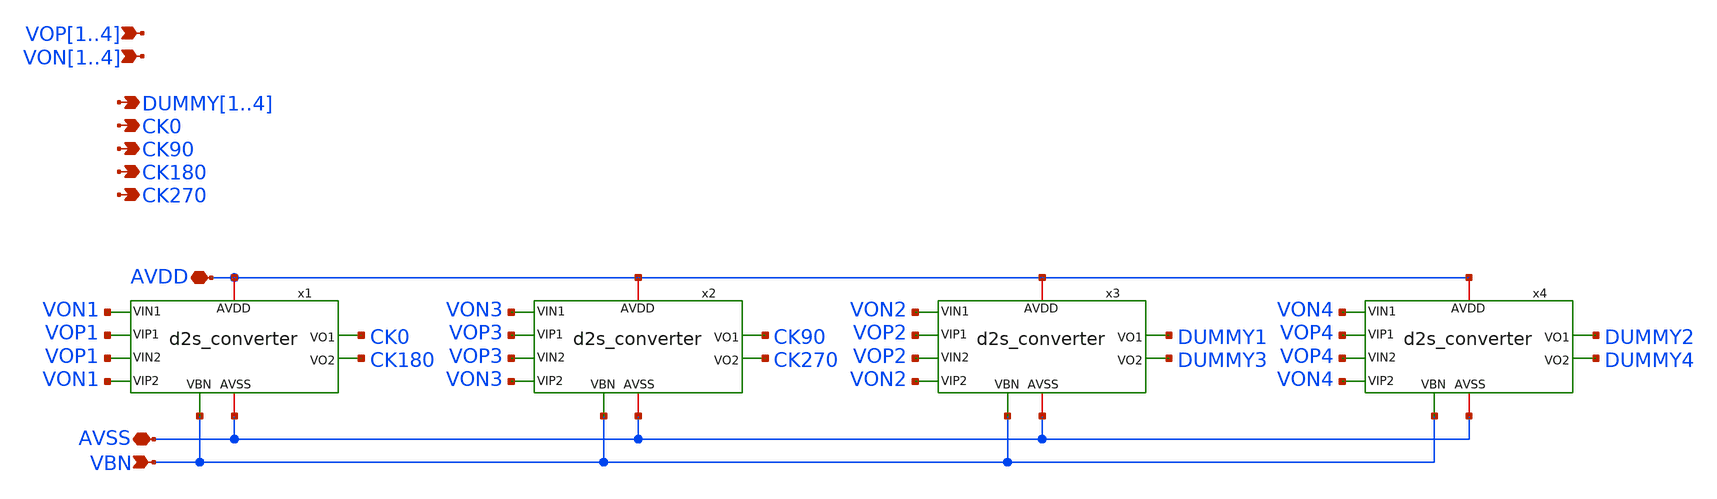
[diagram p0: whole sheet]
** sch_path: designs/libs/core_analog/d2s_top/d2s_top.sch
**.subckt d2s_top VOP1,VOP2,VOP3,VOP4 VON1,VON2,VON3,VON4 VBN DUMMY1,DUMMY2,DUMMY3,DUMMY4 CK0 CK90
*+ CK180 CK270 AVDD AVSS
*.ipin VOP1,VOP2,VOP3,VOP4
*.ipin VON1,VON2,VON3,VON4
*.ipin VBN
*.opin DUMMY1,DUMMY2,DUMMY3,DUMMY4
*.opin CK0
*.opin CK90
*.opin CK180
*.opin CK270
*.iopin AVDD
*.iopin AVSS
x1 AVDD AVSS VON1 VOP1 VBN CK0 VOP1 VON1 CK180 d2s_converter
x2 AVDD AVSS VON3 VOP3 VBN CK90 VOP3 VON3 CK270 d2s_converter
x3 AVDD AVSS VON2 VOP2 VBN DUMMY1 VOP2 VON2 DUMMY3 d2s_converter
x4 AVDD AVSS VON4 VOP4 VBN DUMMY2 VOP4 VON4 DUMMY4 d2s_converter
**.ends

* expanding   symbol:  libs/core_analog/d2s_converter/d2s_converter.sym # of pins=9
** sym_path: designs/libs/core_analog/d2s_converter/d2s_converter.sym
** sch_path: designs/libs/core_analog/d2s_converter/d2s_converter.sch
.subckt d2s_converter AVDD AVSS VIN1 VIP1 VBN VO1 VIN2 VIP2 VO2
*.iopin AVDD
*.iopin AVSS
*.ipin VIN1
*.ipin VIP1
*.opin VO1
*.ipin VBN
*.opin VO2
*.ipin VIN2
*.ipin VIP2
XM2 VOPB1 VIN1 i1 AVSS nfet_03v3 L=0.3u W=0.95u nf=1 ad='int((nf+1)/2) * W/nf * 0.18u' as='int((nf+2)/2) * W/nf * 0.18u'
+ pd='2*int((nf+1)/2) * (W/nf + 0.18u)' ps='2*int((nf+2)/2) * (W/nf + 0.18u)' nrd='0.18u / W' nrs='0.18u / W'
+ sa=0 sb=0 sd=0 m=4
XM4 VOPB1 VOPB1 AVDD AVDD pfet_03v3 L=0.3u W=0.7u nf=1 ad='int((nf+1)/2) * W/nf * 0.18u' as='int((nf+2)/2) * W/nf * 0.18u'
+ pd='2*int((nf+1)/2) * (W/nf + 0.18u)' ps='2*int((nf+2)/2) * (W/nf + 0.18u)' nrd='0.18u / W' nrs='0.18u / W'
+ sa=0 sb=0 sd=0 m=4
XM11 VOB1 VOB1 AVSS AVSS nfet_03v3 L=0.3u W=0.75u nf=1 ad='int((nf+1)/2) * W/nf * 0.18u' as='int((nf+2)/2) * W/nf * 0.18u'
+ pd='2*int((nf+1)/2) * (W/nf + 0.18u)' ps='2*int((nf+2)/2) * (W/nf + 0.18u)' nrd='0.18u / W' nrs='0.18u / W'
+ sa=0 sb=0 sd=0 m=4
XM13 VOB1 VOP1 AVDD AVDD pfet_03v3 L=0.3u W=1u nf=1 ad='int((nf+1)/2) * W/nf * 0.18u' as='int((nf+2)/2) * W/nf * 0.18u'
+ pd='2*int((nf+1)/2) * (W/nf + 0.18u)' ps='2*int((nf+2)/2) * (W/nf + 0.18u)' nrd='0.18u / W' nrs='0.18u / W'
+ sa=0 sb=0 sd=0 m=4
XM1 i1 VBN AVSS AVSS nfet_03v3 L=0.5u W=2.82u nf=1 ad='int((nf+1)/2) * W/nf * 0.18u' as='int((nf+2)/2) * W/nf * 0.18u'
+ pd='2*int((nf+1)/2) * (W/nf + 0.18u)' ps='2*int((nf+2)/2) * (W/nf + 0.18u)' nrd='0.18u / W' nrs='0.18u / W'
+ sa=0 sb=0 sd=0 m=4
x2 AVDD y VO2 AVSS inv
x1 AVDD x VO1 AVSS inv
XM3 VOP1 VIP1 i1 AVSS nfet_03v3 L=0.3u W=0.95u nf=1 ad='int((nf+1)/2) * W/nf * 0.18u' as='int((nf+2)/2) * W/nf * 0.18u'
+ pd='2*int((nf+1)/2) * (W/nf + 0.18u)' ps='2*int((nf+2)/2) * (W/nf + 0.18u)' nrd='0.18u / W' nrs='0.18u / W'
+ sa=0 sb=0 sd=0 m=4
XM7 VONB1 VIP1 i2 AVSS nfet_03v3 L=0.3u W=0.95u nf=1 ad='int((nf+1)/2) * W/nf * 0.18u' as='int((nf+2)/2) * W/nf * 0.18u'
+ pd='2*int((nf+1)/2) * (W/nf + 0.18u)' ps='2*int((nf+2)/2) * (W/nf + 0.18u)' nrd='0.18u / W' nrs='0.18u / W'
+ sa=0 sb=0 sd=0 m=4
XM9 VON1 VIN1 i2 AVSS nfet_03v3 L=0.3u W=0.95u nf=1 ad='int((nf+1)/2) * W/nf * 0.18u' as='int((nf+2)/2) * W/nf * 0.18u'
+ pd='2*int((nf+1)/2) * (W/nf + 0.18u)' ps='2*int((nf+2)/2) * (W/nf + 0.18u)' nrd='0.18u / W' nrs='0.18u / W'
+ sa=0 sb=0 sd=0 m=4
XM5 VOP1 VOPB1 AVDD AVDD pfet_03v3 L=0.3u W=0.7u nf=1 ad='int((nf+1)/2) * W/nf * 0.18u' as='int((nf+2)/2) * W/nf * 0.18u'
+ pd='2*int((nf+1)/2) * (W/nf + 0.18u)' ps='2*int((nf+2)/2) * (W/nf + 0.18u)' nrd='0.18u / W' nrs='0.18u / W'
+ sa=0 sb=0 sd=0 m=4
XM8 VONB1 VONB1 AVDD AVDD pfet_03v3 L=0.3u W=0.7u nf=1 ad='int((nf+1)/2) * W/nf * 0.18u' as='int((nf+2)/2) * W/nf * 0.18u'
+ pd='2*int((nf+1)/2) * (W/nf + 0.18u)' ps='2*int((nf+2)/2) * (W/nf + 0.18u)' nrd='0.18u / W' nrs='0.18u / W'
+ sa=0 sb=0 sd=0 m=4
XM10 VON1 VONB1 AVDD AVDD pfet_03v3 L=0.3u W=0.7u nf=1 ad='int((nf+1)/2) * W/nf * 0.18u' as='int((nf+2)/2) * W/nf * 0.18u'
+ pd='2*int((nf+1)/2) * (W/nf + 0.18u)' ps='2*int((nf+2)/2) * (W/nf + 0.18u)' nrd='0.18u / W' nrs='0.18u / W'
+ sa=0 sb=0 sd=0 m=4
XM15 VOPB2 VIN2 i3 AVSS nfet_03v3 L=0.3u W=0.95u nf=1 ad='int((nf+1)/2) * W/nf * 0.18u' as='int((nf+2)/2) * W/nf * 0.18u'
+ pd='2*int((nf+1)/2) * (W/nf + 0.18u)' ps='2*int((nf+2)/2) * (W/nf + 0.18u)' nrd='0.18u / W' nrs='0.18u / W'
+ sa=0 sb=0 sd=0 m=4
XM16 VOPB2 VOPB2 AVDD AVDD pfet_03v3 L=0.3u W=0.7u nf=1 ad='int((nf+1)/2) * W/nf * 0.18u' as='int((nf+2)/2) * W/nf * 0.18u'
+ pd='2*int((nf+1)/2) * (W/nf + 0.18u)' ps='2*int((nf+2)/2) * (W/nf + 0.18u)' nrd='0.18u / W' nrs='0.18u / W'
+ sa=0 sb=0 sd=0 m=4
XM21 VOP2 VIP2 i3 AVSS nfet_03v3 L=0.3u W=0.95u nf=1 ad='int((nf+1)/2) * W/nf * 0.18u' as='int((nf+2)/2) * W/nf * 0.18u'
+ pd='2*int((nf+1)/2) * (W/nf + 0.18u)' ps='2*int((nf+2)/2) * (W/nf + 0.18u)' nrd='0.18u / W' nrs='0.18u / W'
+ sa=0 sb=0 sd=0 m=4
XM22 VONB2 VIP2 i4 AVSS nfet_03v3 L=0.3u W=0.95u nf=1 ad='int((nf+1)/2) * W/nf * 0.18u' as='int((nf+2)/2) * W/nf * 0.18u'
+ pd='2*int((nf+1)/2) * (W/nf + 0.18u)' ps='2*int((nf+2)/2) * (W/nf + 0.18u)' nrd='0.18u / W' nrs='0.18u / W'
+ sa=0 sb=0 sd=0 m=4
XM23 VON2 VIN2 i4 AVSS nfet_03v3 L=0.3u W=0.95u nf=1 ad='int((nf+1)/2) * W/nf * 0.18u' as='int((nf+2)/2) * W/nf * 0.18u'
+ pd='2*int((nf+1)/2) * (W/nf + 0.18u)' ps='2*int((nf+2)/2) * (W/nf + 0.18u)' nrd='0.18u / W' nrs='0.18u / W'
+ sa=0 sb=0 sd=0 m=4
XM24 VOP2 VOPB2 AVDD AVDD pfet_03v3 L=0.3u W=0.7u nf=1 ad='int((nf+1)/2) * W/nf * 0.18u' as='int((nf+2)/2) * W/nf * 0.18u'
+ pd='2*int((nf+1)/2) * (W/nf + 0.18u)' ps='2*int((nf+2)/2) * (W/nf + 0.18u)' nrd='0.18u / W' nrs='0.18u / W'
+ sa=0 sb=0 sd=0 m=4
XM27 VONB2 VONB2 AVDD AVDD pfet_03v3 L=0.3u W=0.7u nf=1 ad='int((nf+1)/2) * W/nf * 0.18u' as='int((nf+2)/2) * W/nf * 0.18u'
+ pd='2*int((nf+1)/2) * (W/nf + 0.18u)' ps='2*int((nf+2)/2) * (W/nf + 0.18u)' nrd='0.18u / W' nrs='0.18u / W'
+ sa=0 sb=0 sd=0 m=4
XM28 VON2 VONB2 AVDD AVDD pfet_03v3 L=0.3u W=0.7u nf=1 ad='int((nf+1)/2) * W/nf * 0.18u' as='int((nf+2)/2) * W/nf * 0.18u'
+ pd='2*int((nf+1)/2) * (W/nf + 0.18u)' ps='2*int((nf+2)/2) * (W/nf + 0.18u)' nrd='0.18u / W' nrs='0.18u / W'
+ sa=0 sb=0 sd=0 m=4
XM12 x VOB1 AVSS AVSS nfet_03v3 L=0.3u W=0.75u nf=1 ad='int((nf+1)/2) * W/nf * 0.18u' as='int((nf+2)/2) * W/nf * 0.18u'
+ pd='2*int((nf+1)/2) * (W/nf + 0.18u)' ps='2*int((nf+2)/2) * (W/nf + 0.18u)' nrd='0.18u / W' nrs='0.18u / W'
+ sa=0 sb=0 sd=0 m=4
XM14 x VON1 AVDD AVDD pfet_03v3 L=0.3u W=1u nf=1 ad='int((nf+1)/2) * W/nf * 0.18u' as='int((nf+2)/2) * W/nf * 0.18u'
+ pd='2*int((nf+1)/2) * (W/nf + 0.18u)' ps='2*int((nf+2)/2) * (W/nf + 0.18u)' nrd='0.18u / W' nrs='0.18u / W'
+ sa=0 sb=0 sd=0 m=4
XM17 VOB2 VOB2 AVSS AVSS nfet_03v3 L=0.3u W=0.75u nf=1 ad='int((nf+1)/2) * W/nf * 0.18u' as='int((nf+2)/2) * W/nf * 0.18u'
+ pd='2*int((nf+1)/2) * (W/nf + 0.18u)' ps='2*int((nf+2)/2) * (W/nf + 0.18u)' nrd='0.18u / W' nrs='0.18u / W'
+ sa=0 sb=0 sd=0 m=4
XM18 VOB2 VOP2 AVDD AVDD pfet_03v3 L=0.3u W=1u nf=1 ad='int((nf+1)/2) * W/nf * 0.18u' as='int((nf+2)/2) * W/nf * 0.18u'
+ pd='2*int((nf+1)/2) * (W/nf + 0.18u)' ps='2*int((nf+2)/2) * (W/nf + 0.18u)' nrd='0.18u / W' nrs='0.18u / W'
+ sa=0 sb=0 sd=0 m=4
XM25 y VOB2 AVSS AVSS nfet_03v3 L=0.3u W=0.75u nf=1 ad='int((nf+1)/2) * W/nf * 0.18u' as='int((nf+2)/2) * W/nf * 0.18u'
+ pd='2*int((nf+1)/2) * (W/nf + 0.18u)' ps='2*int((nf+2)/2) * (W/nf + 0.18u)' nrd='0.18u / W' nrs='0.18u / W'
+ sa=0 sb=0 sd=0 m=4
XM26 y VON2 AVDD AVDD pfet_03v3 L=0.3u W=1u nf=1 ad='int((nf+1)/2) * W/nf * 0.18u' as='int((nf+2)/2) * W/nf * 0.18u'
+ pd='2*int((nf+1)/2) * (W/nf + 0.18u)' ps='2*int((nf+2)/2) * (W/nf + 0.18u)' nrd='0.18u / W' nrs='0.18u / W'
+ sa=0 sb=0 sd=0 m=4
XM6 i2 VBN AVSS AVSS nfet_03v3 L=0.5u W=2.82u nf=1 ad='int((nf+1)/2) * W/nf * 0.18u' as='int((nf+2)/2) * W/nf * 0.18u'
+ pd='2*int((nf+1)/2) * (W/nf + 0.18u)' ps='2*int((nf+2)/2) * (W/nf + 0.18u)' nrd='0.18u / W' nrs='0.18u / W'
+ sa=0 sb=0 sd=0 m=4
XM19 i3 VBN AVSS AVSS nfet_03v3 L=0.5u W=2.82u nf=1 ad='int((nf+1)/2) * W/nf * 0.18u' as='int((nf+2)/2) * W/nf * 0.18u'
+ pd='2*int((nf+1)/2) * (W/nf + 0.18u)' ps='2*int((nf+2)/2) * (W/nf + 0.18u)' nrd='0.18u / W' nrs='0.18u / W'
+ sa=0 sb=0 sd=0 m=4
XM20 i4 VBN AVSS AVSS nfet_03v3 L=0.5u W=2.82u nf=1 ad='int((nf+1)/2) * W/nf * 0.18u' as='int((nf+2)/2) * W/nf * 0.18u'
+ pd='2*int((nf+1)/2) * (W/nf + 0.18u)' ps='2*int((nf+2)/2) * (W/nf + 0.18u)' nrd='0.18u / W' nrs='0.18u / W'
+ sa=0 sb=0 sd=0 m=4
.ends


* expanding   symbol:  libs/core_analog/inv/inv.sym # of pins=4
** sym_path: designs/libs/core_analog/inv/inv.sym
** sch_path: designs/libs/core_analog/inv/inv.sch
.subckt inv AVDD IN OUT AVSS
*.ipin IN
*.iopin AVDD
*.iopin AVSS
*.opin OUT
XM1 OUT IN AVDD AVDD pfet_03v3 L=0.28u W=0.9u nf=1 ad='int((nf+1)/2) * W/nf * 0.18u' as='int((nf+2)/2) * W/nf * 0.18u'
+ pd='2*int((nf+1)/2) * (W/nf + 0.18u)' ps='2*int((nf+2)/2) * (W/nf + 0.18u)' nrd='0.18u / W' nrs='0.18u / W'
+ sa=0 sb=0 sd=0 m=1
XM2 OUT IN AVSS AVSS nfet_03v3 L=0.28u W=0.3u nf=1 ad='int((nf+1)/2) * W/nf * 0.18u' as='int((nf+2)/2) * W/nf * 0.18u'
+ pd='2*int((nf+1)/2) * (W/nf + 0.18u)' ps='2*int((nf+2)/2) * (W/nf + 0.18u)' nrd='0.18u / W' nrs='0.18u / W'
+ sa=0 sb=0 sd=0 m=1
.ends

.end
